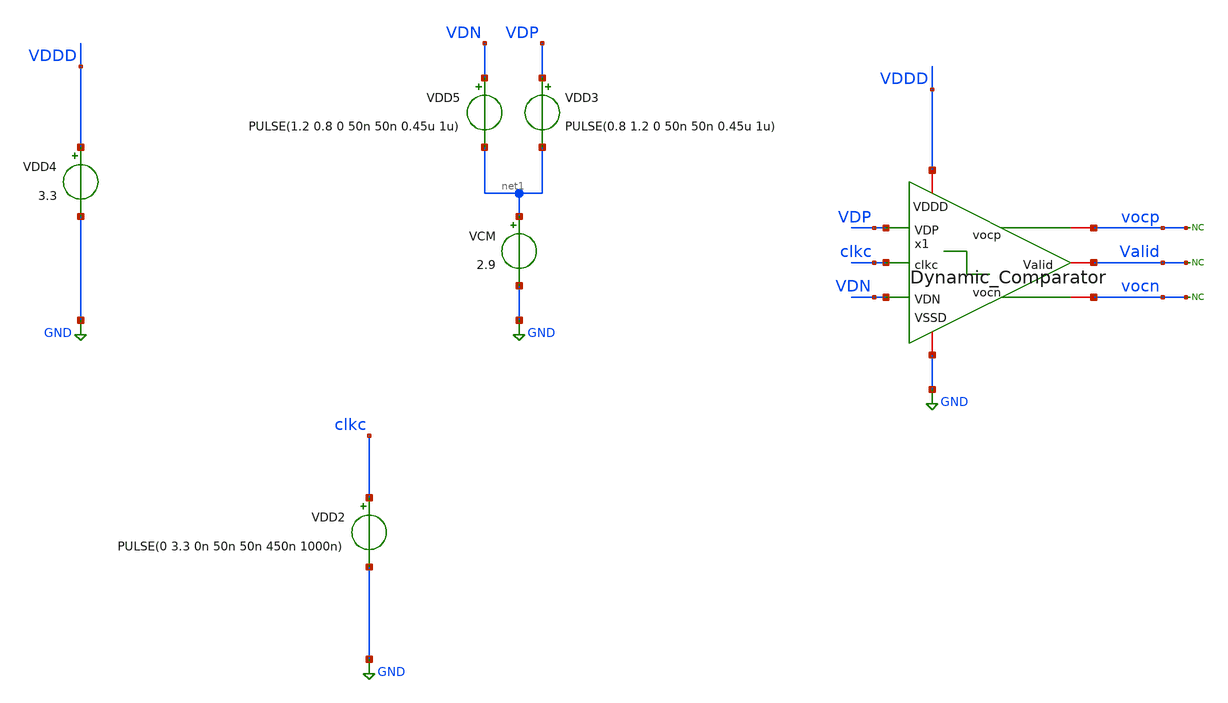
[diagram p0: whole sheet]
** sch_path: SAR_ADC/Dynamic_Comparator/xschem/Dynamic_Comparator_tb.sch
**.subckt Dynamic_Comparator_tb
VDD4 VDDD GND 3.3
VDD2 clkc GND PULSE(0 3.3 0n 50n 50n 450n 1000n)
VDD3 VDP net1 PULSE(0.8 1.2 0 50n 50n 0.45u 1u)
VCM net1 GND 2.9
VDD5 VDN net1 PULSE(1.2 0.8 0 50n 50n 0.45u 1u)
* noconn Valid
* noconn vocp
* noconn vocn
x1 vocp vocn VDDD GND VDP VDN Valid clkc Dynamic_Comparator
**** begin user architecture code



*Parameters

.options TEMP = 50.0
.lib /home/electrica/Documents/gf180_projects/pdk/gf180mcuC/libs.tech/ngspice/sm141064.ngspice typical
.include /home/electrica/Documents/gf180_projects/pdk/gf180mcuC/libs.tech/ngspice/design.ngspice

*Data to save
.save all

* Simulation
.control
tran 0.1n 5u
setplot dc1
plot V(VDP)+20 V(VDN)+20 V(clkc)+20 V(.x1.aN)+16 V(.x1.aP)+16 V(.x1.dP)+12 V(.x1.dN)+8
set filetype = ascii
write Dynamic_Comparator_tb_tran.raw

reset
unset filetype
op
save all
write Dynamic_Comparator_tb.raw


.endc
.end


**** end user architecture code
**.ends
.GLOBAL GND
.end
